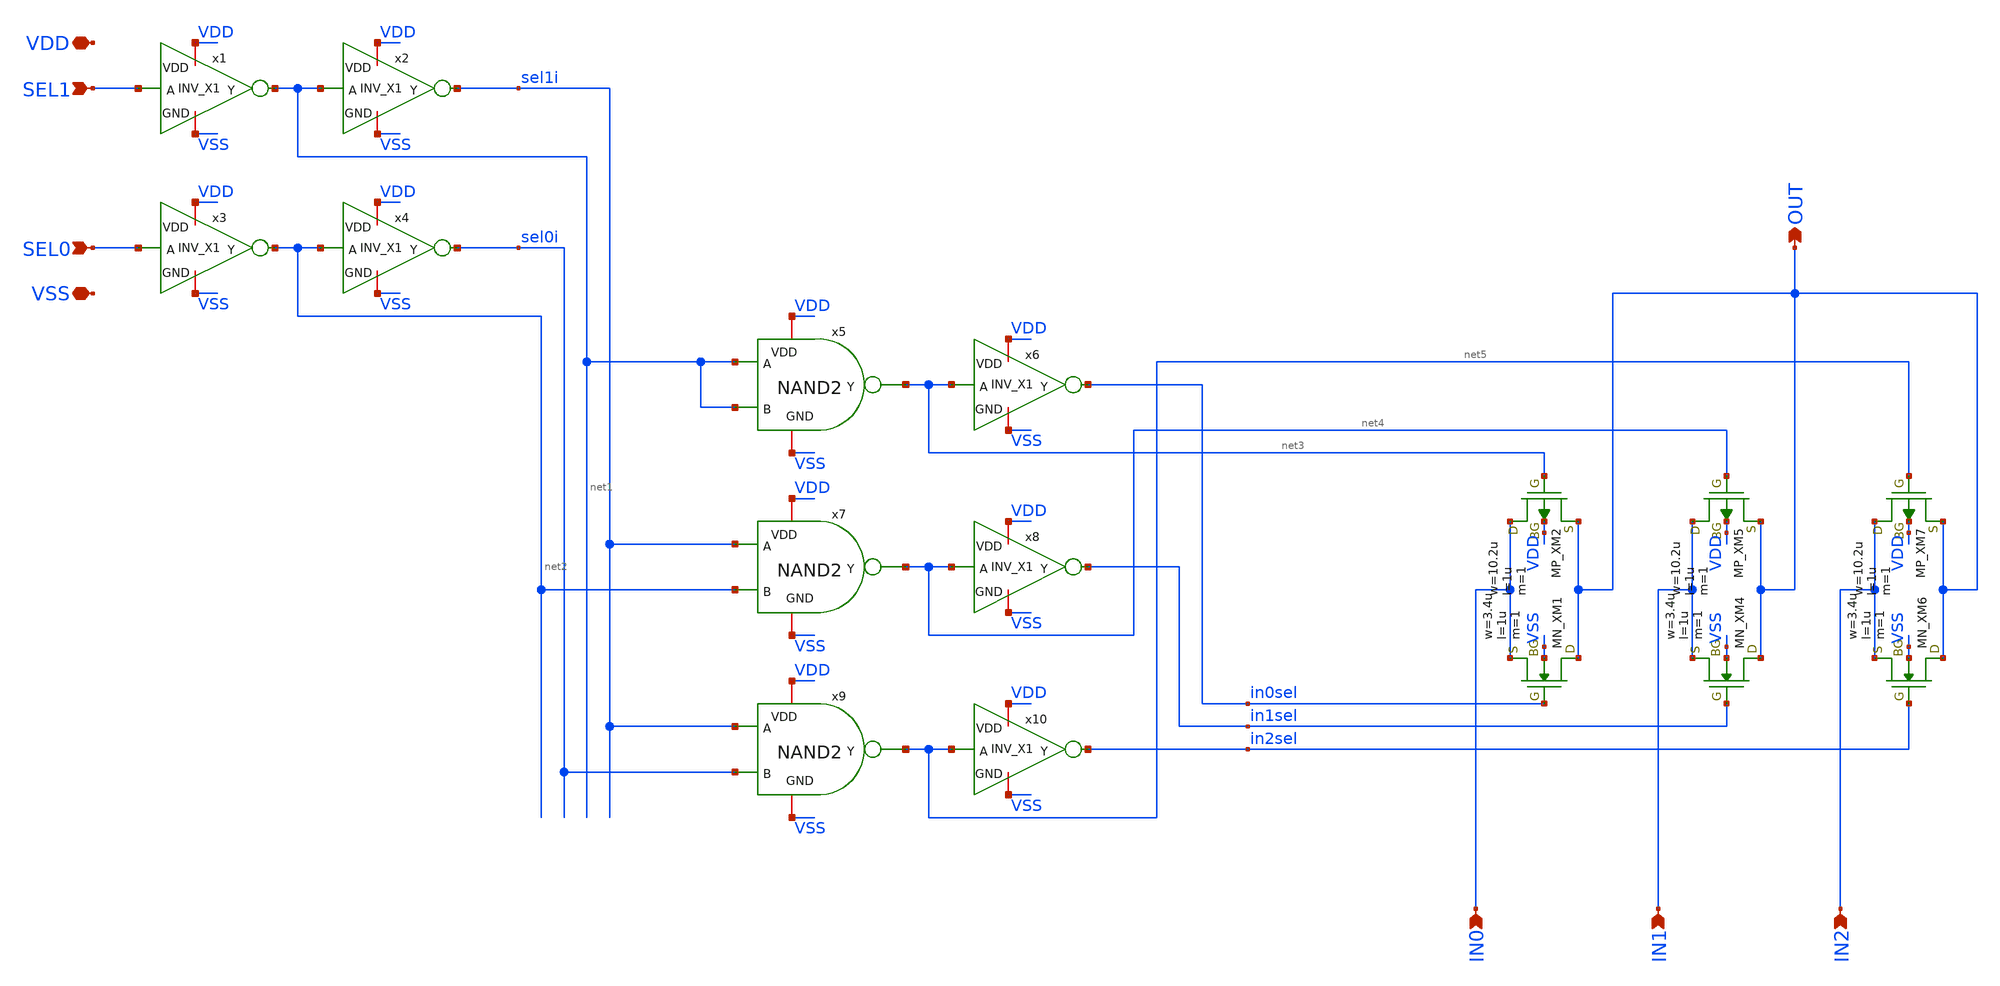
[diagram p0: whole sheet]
** sch_path: member_project/BGR/Maehashi/design/sel.sch
**.subckt sel VDD SEL1 VSS IN0 IN1 IN2 OUT SEL0
*.iopin VDD
*.ipin SEL1
*.iopin VSS
*.ipin IN0
*.ipin IN1
*.ipin IN2
*.opin OUT
*.ipin SEL0
XXM1 OUT in0sel IN0 VSS NMOS w=3.4u l=1u as=0 ad=0 ps=0 pd=0 nrd=0 nrs=0 m=1
XXM2 IN0 net3 OUT VDD PMOS w=10.2u l=1u as=0 ad=0 ps=0 pd=0 nrd=0 nrs=0 m=1
XXM4 OUT in1sel IN1 VSS NMOS w=3.4u l=1u as=0 ad=0 ps=0 pd=0 nrd=0 nrs=0 m=1
XXM5 IN1 net4 OUT VDD PMOS w=10.2u l=1u as=0 ad=0 ps=0 pd=0 nrd=0 nrs=0 m=1
XXM6 OUT in2sel IN2 VSS NMOS w=3.4u l=1u as=0 ad=0 ps=0 pd=0 nrd=0 nrs=0 m=1
XXM7 IN2 net5 OUT VDD PMOS w=10.2u l=1u as=0 ad=0 ps=0 pd=0 nrd=0 nrs=0 m=1
x1 VDD SEL1 net1 VSS INV_X1
x2 VDD net1 sel1i VSS INV_X1
x3 VDD SEL0 net2 VSS INV_X1
x4 VDD net2 sel0i VSS INV_X1
x5 VDD net3 net1 net1 VSS NAND2
x6 VDD net3 in0sel VSS INV_X1
x7 VDD net4 sel1i net2 VSS NAND2
x8 VDD net4 in1sel VSS INV_X1
x9 VDD net5 sel1i sel0i VSS NAND2
x10 VDD net5 in2sel VSS INV_X1
**.ends

* expanding   symbol:  IP62_5_stdcell/INV_X1.sym # of pins=4
** sym_path: IP62_5_stdcell/INV_X1.sym
** sch_path: IP62_5_stdcell/INV_X1.sch
.subckt INV_X1 VDD A Y GND
*.ipin A
*.opin Y
*.iopin GND
*.iopin VDD
XM7 Y A VDD VDD PMOS w=10.2u l=1u as=0 ad=0 ps=0 pd=0 nrd=0 nrs=0 m=1
XM2 Y A GND GND NMOS w=3.4u l=1u as=0 ad=0 ps=0 pd=0 nrd=0 nrs=0 m=1
.ends


* expanding   symbol:  IP62_5_stdcell/NAND2.sym # of pins=5
** sym_path: IP62_5_stdcell/NAND2.sym
** sch_path: IP62_5_stdcell/NAND2.sch
.subckt NAND2 VDD Y A B GND
*.ipin B
*.ipin A
*.opin Y
*.iopin GND
*.iopin VDD
XM7 Y A VDD VDD PMOS w=10.2u l=1u as=0 ad=0 ps=0 pd=0 nrd=0 nrs=0 m=1
XM1 Y B VDD VDD PMOS w=10.2u l=1u as=0 ad=0 ps=0 pd=0 nrd=0 nrs=0 m=1
XM2 Y B net1 GND NMOS w=3.4u l=1u as=0 ad=0 ps=0 pd=0 nrd=0 nrs=0 m=1
XM3 net1 A GND GND NMOS w=3.4u l=1u as=0 ad=0 ps=0 pd=0 nrd=0 nrs=0 m=1
.ends

.end
